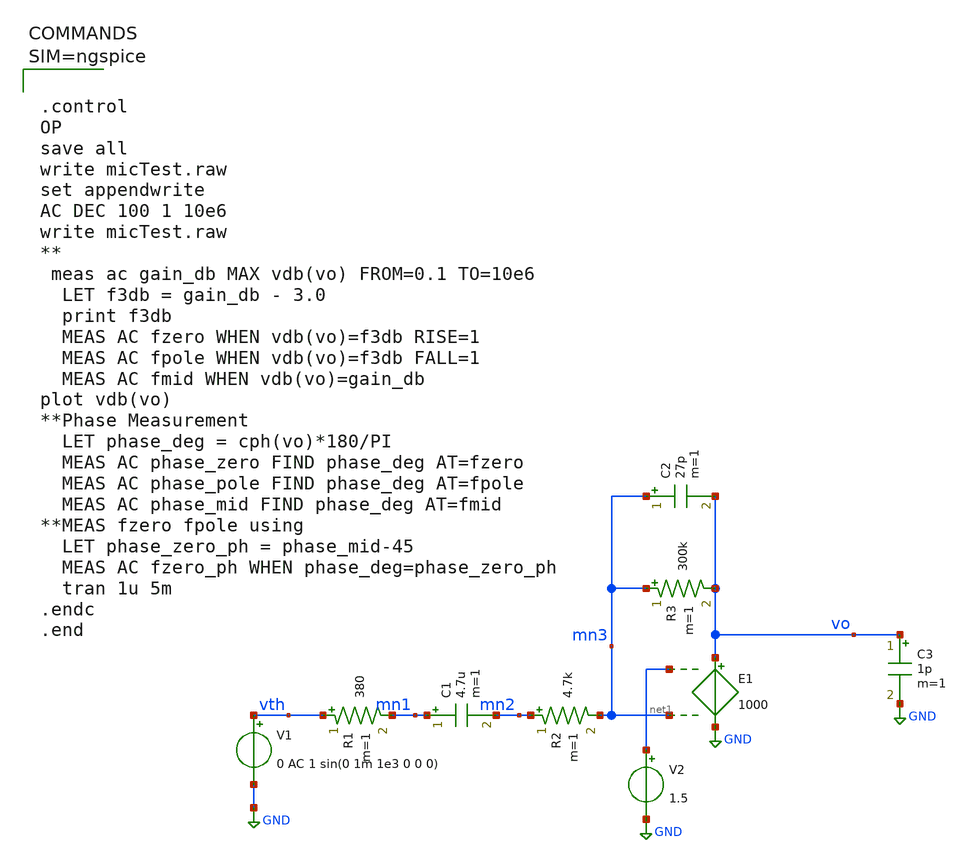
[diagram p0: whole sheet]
** sch_path: xschem/micTest.sch
**.subckt micTest
V1 vth GND 0 AC 1 sin(0 1m 1e3 0 0 0)
R1 vth mn1 380 m=1
C1 mn1 mn2 4.7u m=1
R2 mn2 mn3 4.7k m=1
E1 vo GND net1 mn3 1000
R3 mn3 vo 300k m=1
C2 mn3 vo 27p m=1
V2 net1 GND 1.5
C3 vo GND 1p m=1
**** begin user architecture code



.control
OP
save all
write micTest.raw
set appendwrite
AC DEC 100 1 10e6
write micTest.raw
**
 meas ac gain_db MAX vdb(vo) FROM=0.1 TO=10e6
  LET f3db = gain_db - 3.0
  print f3db
  MEAS AC fzero WHEN vdb(vo)=f3db RISE=1
  MEAS AC fpole WHEN vdb(vo)=f3db FALL=1
  MEAS AC fmid WHEN vdb(vo)=gain_db
plot vdb(vo)
**Phase Measurement
  LET phase_deg = cph(vo)*180/PI
  MEAS AC phase_zero FIND phase_deg AT=fzero
  MEAS AC phase_pole FIND phase_deg AT=fpole
  MEAS AC phase_mid FIND phase_deg AT=fmid
**MEAS fzero fpole using
  LET phase_zero_ph = phase_mid-45
  MEAS AC fzero_ph WHEN phase_deg=phase_zero_ph
  tran 1u 5m
.endc
.end



**** end user architecture code
**.ends
.GLOBAL GND
.end
